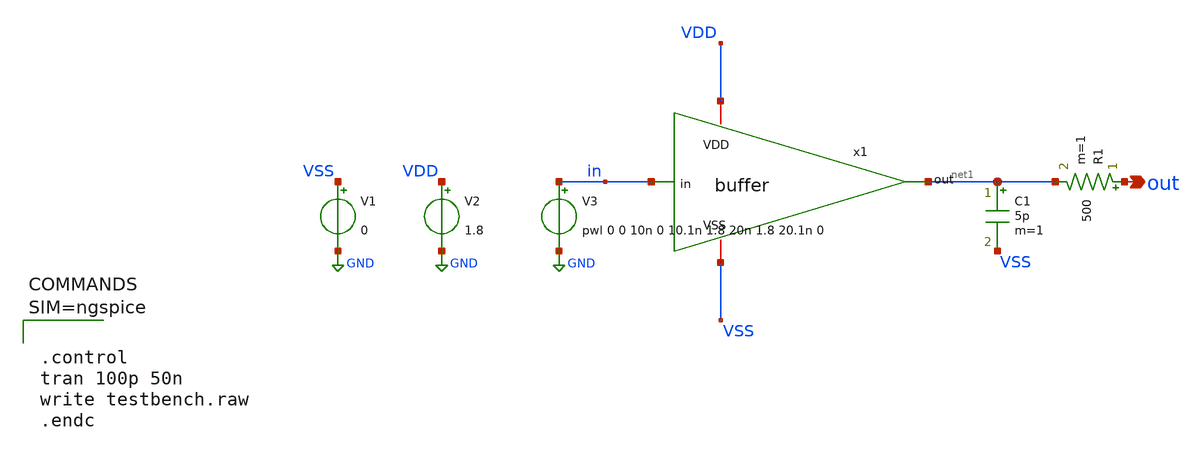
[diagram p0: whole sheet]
** sch_path: xschem/testbench.sch
**.subckt testbench out
*.opin out
x1 VDD VSS net1 in buffer
V1 VSS GND 0
V2 VDD GND 1.8
V3 in GND pwl 0 0 10n 0 10.1n 1.8 20n 1.8 20.1n 0
C1 net1 VSS 5p m=1
R1 out net1 500 m=1
**** begin user architecture code

** opencircuitdesign pdks install
.lib $::SKYWATER_MODELS/sky130.lib.spice tt





.control
tran 100p 50n
write testbench.raw
.endc



**** end user architecture code
**.ends
.GLOBAL GND
.end
